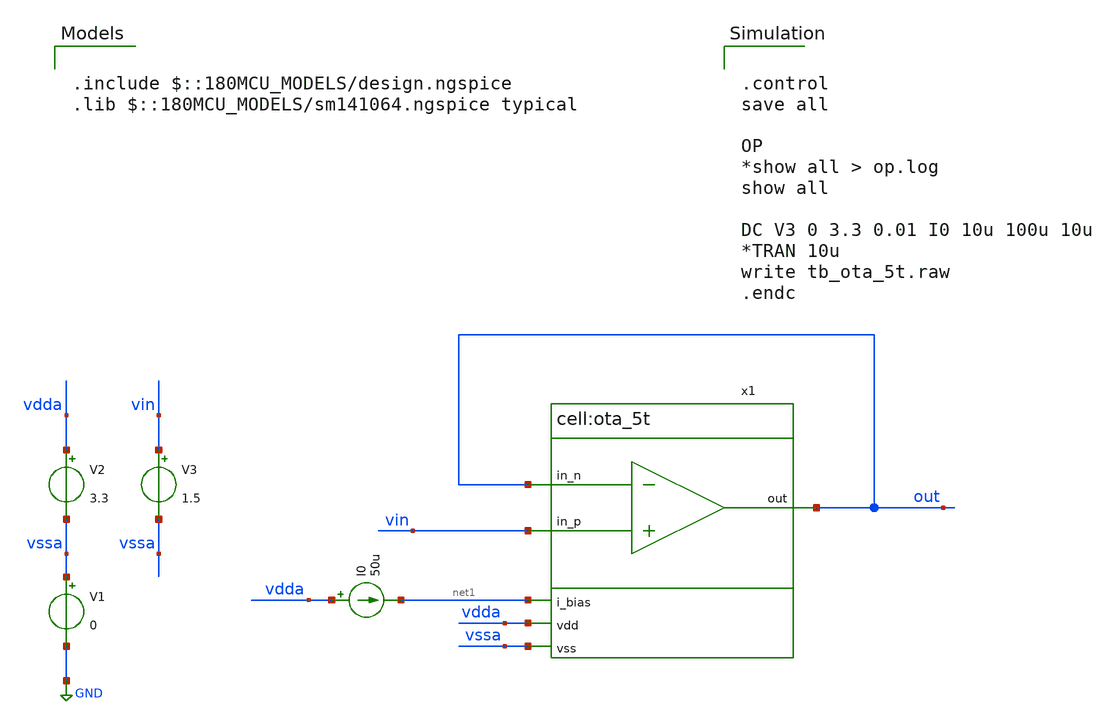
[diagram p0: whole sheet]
** sch_path: designs/libs/tb_analog/tb_ota_5t_dc/tb_ota_5t_dc.sch
**.subckt tb_ota_5t_dc
V1 vssa GND 0
V2 vdda vssa 3.3
I0 vdda net1 50u
V3 vin vssa 1.5
x1 vdda out vin out net1 vssa ota_5t
**** begin user architecture code


.control
save all

OP
*show all > op.log
show all

DC V3 0 3.3 0.01 I0 10u 100u 10u
*TRAN 10u
write tb_ota_5t.raw
.endc



.include $::180MCU_MODELS/design.ngspice
.lib $::180MCU_MODELS/sm141064.ngspice typical

**** end user architecture code
**.ends

* expanding   symbol:  libs/core_analog/ota_5t/ota_5t.sym # of pins=6
** sym_path: libs/core_analog/ota_5t/ota_5t.sym
** sch_path: libs/core_analog/ota_5t/ota_5t.sch
.subckt ota_5t vdd out in_p in_n i_bias vss
*.ipin in_p
*.ipin in_n
*.ipin i_bias
*.ipin vdd
*.ipin vss
*.opin out
XM1 net2 i_bias vss vss nfet_03v3 L=0.28u W=6u nf=2 ad='int((nf+1)/2) * W/nf * 0.18u' as='int((nf+2)/2) * W/nf * 0.18u'
+ pd='2*int((nf+1)/2) * (W/nf + 0.18u)' ps='2*int((nf+2)/2) * (W/nf + 0.18u)' nrd='0.18u / W' nrs='0.18u / W'
+ sa=0 sb=0 sd=0 m=2
XM2 i_bias i_bias vss vss nfet_03v3 L=0.28u W=6u nf=2 ad='int((nf+1)/2) * W/nf * 0.18u' as='int((nf+2)/2) * W/nf * 0.18u'
+ pd='2*int((nf+1)/2) * (W/nf + 0.18u)' ps='2*int((nf+2)/2) * (W/nf + 0.18u)' nrd='0.18u / W' nrs='0.18u / W'
+ sa=0 sb=0 sd=0 m=1
XM3 net1 in_p net2 vss nfet_03v3 L=0.28u W=6u nf=2 ad='int((nf+1)/2) * W/nf * 0.18u' as='int((nf+2)/2) * W/nf * 0.18u'
+ pd='2*int((nf+1)/2) * (W/nf + 0.18u)' ps='2*int((nf+2)/2) * (W/nf + 0.18u)' nrd='0.18u / W' nrs='0.18u / W'
+ sa=0 sb=0 sd=0 m=1
XM4 out in_n net2 vss nfet_03v3 L=0.28u W=6u nf=2 ad='int((nf+1)/2) * W/nf * 0.18u' as='int((nf+2)/2) * W/nf * 0.18u'
+ pd='2*int((nf+1)/2) * (W/nf + 0.18u)' ps='2*int((nf+2)/2) * (W/nf + 0.18u)' nrd='0.18u / W' nrs='0.18u / W'
+ sa=0 sb=0 sd=0 m=1
XM5 out net1 vdd vdd pfet_03v3 L=0.28u W=6u nf=2 ad='int((nf+1)/2) * W/nf * 0.18u' as='int((nf+2)/2) * W/nf * 0.18u'
+ pd='2*int((nf+1)/2) * (W/nf + 0.18u)' ps='2*int((nf+2)/2) * (W/nf + 0.18u)' nrd='0.18u / W' nrs='0.18u / W'
+ sa=0 sb=0 sd=0 m=3
XM6 net1 net1 vdd vdd pfet_03v3 L=0.28u W=6u nf=2 ad='int((nf+1)/2) * W/nf * 0.18u' as='int((nf+2)/2) * W/nf * 0.18u'
+ pd='2*int((nf+1)/2) * (W/nf + 0.18u)' ps='2*int((nf+2)/2) * (W/nf + 0.18u)' nrd='0.18u / W' nrs='0.18u / W'
+ sa=0 sb=0 sd=0 m=3
.ends

.GLOBAL GND
.end
